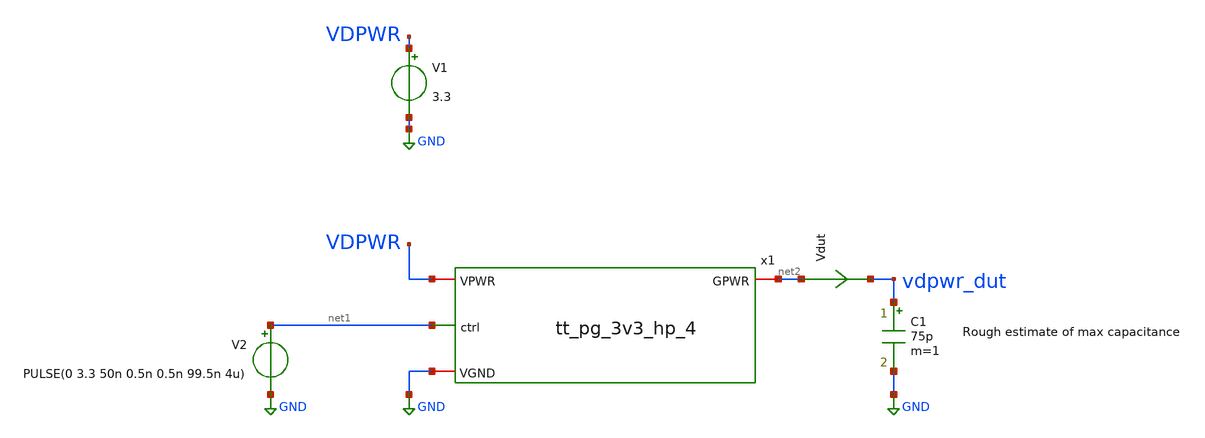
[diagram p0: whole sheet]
** sch_path: pg/gf180mcuD/tt_pg_3v3_hp_4/xschem/tb_switch.sch
**.subckt tb_switch
x1 GND VDPWR net1 net2 tt_pg_3v3_hp_4
V1 VDPWR GND 3.3
.save i(v1)
C1 vdpwr_dut GND 75p m=1
V2 net1 GND PULSE(0 3.3 50n 0.5n 0.5n 99.5n 4u)
Vdut net2 vdpwr_dut 0
.save i(vdut)
**** begin user architecture code


.param mc_mm_switch=0
.control
save all
tran 50p 5u
plot vdpwr_dut
plot vdpwr_dut x1.ctrl_n xlimit 50n 60n
*quit 0
.endc
.end



.include design.ngspice
.lib sm141064.ngspice typical

**** end user architecture code
**.ends

* expanding   symbol:  tt_pg_3v3_hp_4.sym # of pins=4
** sym_path: pg/gf180mcuD/tt_pg_3v3_hp_4/xschem/tt_pg_3v3_hp_4.sym
** sch_path: pg/gf180mcuD/tt_pg_3v3_hp_4/xschem/tt_pg_3v3_hp_4.sch
.subckt tt_pg_3v3_hp_4 VGND VPWR ctrl GPWR
*.ipin ctrl
*.iopin VPWR
*.iopin VGND
*.iopin GPWR
x[1] VGND GPWR ctrl_n discharge_3v3
x[2] VGND GPWR ctrl_n discharge_3v3
XM1 ctrl_n ctrl VGND VGND nfet_03v3 L=0.28u W=11.0u nf=4 ad='int((nf+1)/2) * W/nf * 0.18u' as='int((nf+2)/2) * W/nf * 0.18u'
+ pd='2*int((nf+1)/2) * (W/nf + 0.18u)' ps='2*int((nf+2)/2) * (W/nf + 0.18u)' nrd='0.18u / W' nrs='0.18u / W'
+ sa=0 sb=0 sd=0 m=1 par=1
XM2 ctrl_n ctrl VPWR VPWR pfet_03v3 L=0.28u W=20.68u nf=4 ad='int((nf+1)/2) * W/nf * 0.18u' as='int((nf+2)/2) * W/nf * 0.18u'
+ pd='2*int((nf+1)/2) * (W/nf + 0.18u)' ps='2*int((nf+2)/2) * (W/nf + 0.18u)' nrd='0.18u / W' nrs='0.18u / W'
+ sa=0 sb=0 sd=0 m=1 par=1
XM3 GPWR ctrl_n VPWR VPWR pfet_03v3 L=0.28u W=7667u nf=902 ad='int((nf+1)/2) * W/nf * 0.18u' as='int((nf+2)/2) * W/nf * 0.18u'
+ pd='2*int((nf+1)/2) * (W/nf + 0.18u)' ps='2*int((nf+2)/2) * (W/nf + 0.18u)' nrd='0.18u / W' nrs='0.18u / W'
+ sa=0 sb=0 sd=0 m=1 par=1
.ends


* expanding   symbol:  discharge_3v3.sym # of pins=3
** sym_path: pg/gf180mcuD/common/xschem/discharge_3v3.sym
** sch_path: pg/gf180mcuD/common/xschem/discharge_3v3.sch
.subckt discharge_3v3 VGND GPWR gate
*.iopin GPWR
*.iopin VGND
*.ipin gate
XM1 GPWR gate net3 VGND nfet_03v3 L=0.6u W=0.99u nf=1 ad='int((nf+1)/2) * W/nf * 0.18u' as='int((nf+2)/2) * W/nf * 0.18u'
+ pd='2*int((nf+1)/2) * (W/nf + 0.18u)' ps='2*int((nf+2)/2) * (W/nf + 0.18u)' nrd='0.18u / W' nrs='0.18u / W'
+ sa=0 sb=0 sd=0 m=1 par=1
XM2 net3 gate net2 VGND nfet_03v3 L=0.6u W=0.99u nf=1 ad='int((nf+1)/2) * W/nf * 0.18u' as='int((nf+2)/2) * W/nf * 0.18u'
+ pd='2*int((nf+1)/2) * (W/nf + 0.18u)' ps='2*int((nf+2)/2) * (W/nf + 0.18u)' nrd='0.18u / W' nrs='0.18u / W'
+ sa=0 sb=0 sd=0 m=1 par=1
XM3 net2 gate net1 VGND nfet_03v3 L=0.6u W=0.99u nf=1 ad='int((nf+1)/2) * W/nf * 0.18u' as='int((nf+2)/2) * W/nf * 0.18u'
+ pd='2*int((nf+1)/2) * (W/nf + 0.18u)' ps='2*int((nf+2)/2) * (W/nf + 0.18u)' nrd='0.18u / W' nrs='0.18u / W'
+ sa=0 sb=0 sd=0 m=1 par=1
XM4 net1 gate VGND VGND nfet_03v3 L=0.6u W=0.99u nf=1 ad='int((nf+1)/2) * W/nf * 0.18u' as='int((nf+2)/2) * W/nf * 0.18u'
+ pd='2*int((nf+1)/2) * (W/nf + 0.18u)' ps='2*int((nf+2)/2) * (W/nf + 0.18u)' nrd='0.18u / W' nrs='0.18u / W'
+ sa=0 sb=0 sd=0 m=1 par=1
XM5 GPWR gate net6 VGND nfet_03v3 L=0.6u W=0.99u nf=1 ad='int((nf+1)/2) * W/nf * 0.18u' as='int((nf+2)/2) * W/nf * 0.18u'
+ pd='2*int((nf+1)/2) * (W/nf + 0.18u)' ps='2*int((nf+2)/2) * (W/nf + 0.18u)' nrd='0.18u / W' nrs='0.18u / W'
+ sa=0 sb=0 sd=0 m=1 par=1
XM6 net6 gate net5 VGND nfet_03v3 L=0.6u W=0.99u nf=1 ad='int((nf+1)/2) * W/nf * 0.18u' as='int((nf+2)/2) * W/nf * 0.18u'
+ pd='2*int((nf+1)/2) * (W/nf + 0.18u)' ps='2*int((nf+2)/2) * (W/nf + 0.18u)' nrd='0.18u / W' nrs='0.18u / W'
+ sa=0 sb=0 sd=0 m=1 par=1
XM7 net5 gate net4 VGND nfet_03v3 L=0.6u W=0.99u nf=1 ad='int((nf+1)/2) * W/nf * 0.18u' as='int((nf+2)/2) * W/nf * 0.18u'
+ pd='2*int((nf+1)/2) * (W/nf + 0.18u)' ps='2*int((nf+2)/2) * (W/nf + 0.18u)' nrd='0.18u / W' nrs='0.18u / W'
+ sa=0 sb=0 sd=0 m=1 par=1
XM8 net4 gate VGND VGND nfet_03v3 L=0.6u W=0.99u nf=1 ad='int((nf+1)/2) * W/nf * 0.18u' as='int((nf+2)/2) * W/nf * 0.18u'
+ pd='2*int((nf+1)/2) * (W/nf + 0.18u)' ps='2*int((nf+2)/2) * (W/nf + 0.18u)' nrd='0.18u / W' nrs='0.18u / W'
+ sa=0 sb=0 sd=0 m=1 par=1
.ends

.GLOBAL GND
.end
